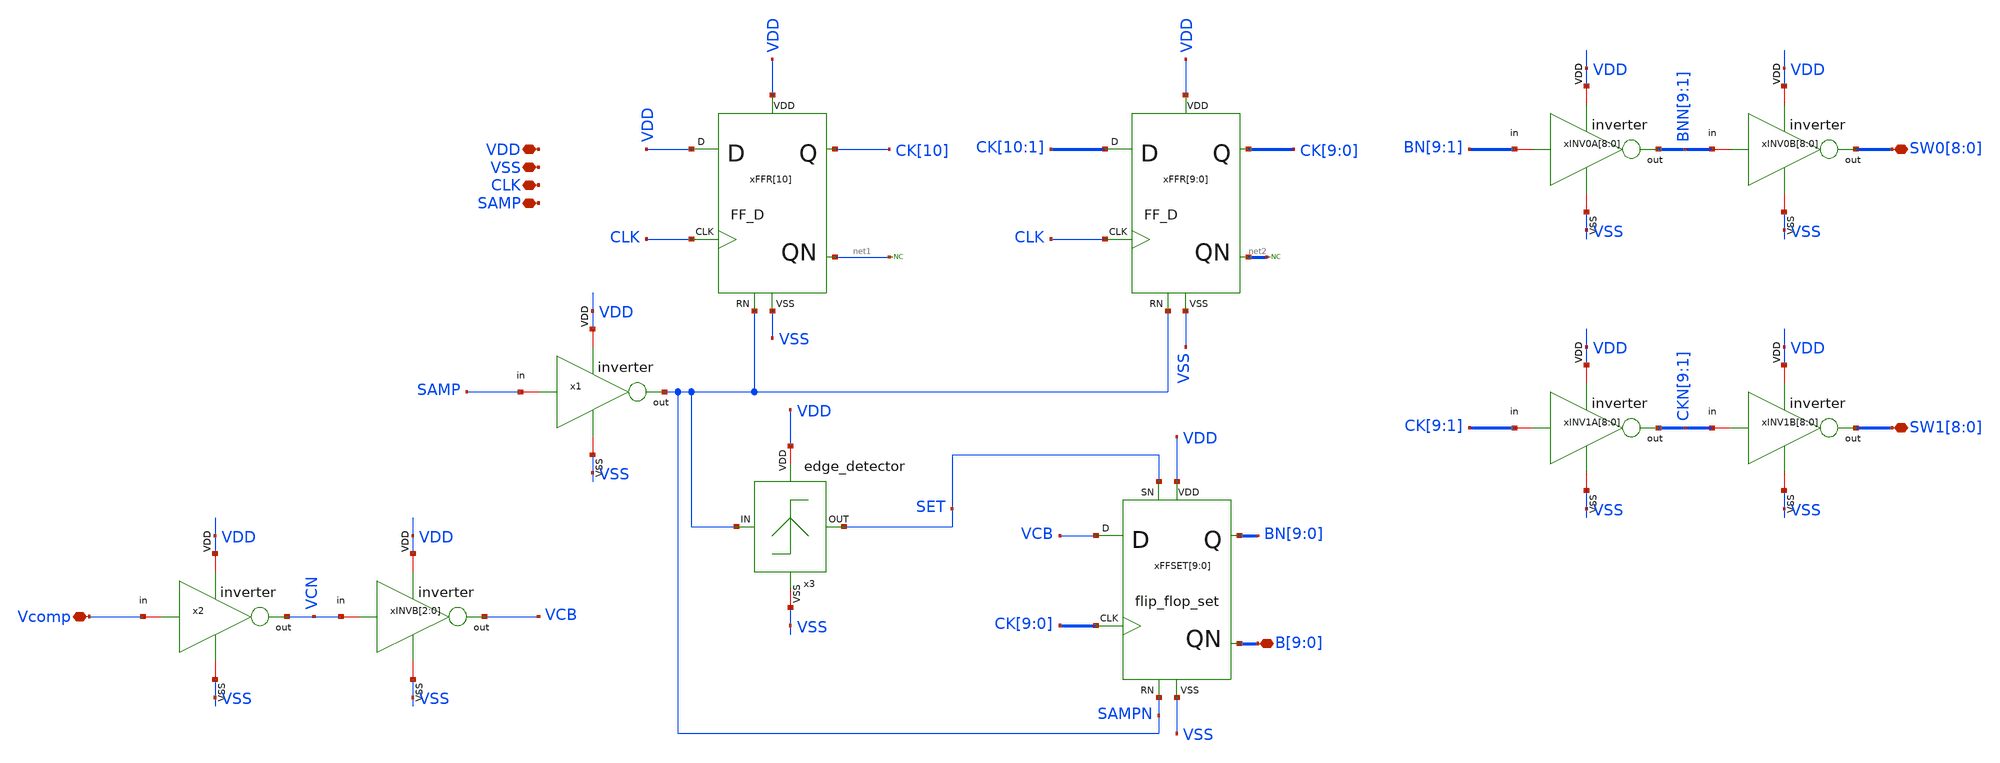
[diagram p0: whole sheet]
** sch_path: designs/sar_adc/digital/logica_digital_TOP/xschem/logica_digital_TOP.sch
**.subckt logica_digital_TOP VDD VSS SAMP CLK Vcomp
*+ B[9],B[8],B[7],B[6],B[5],B[4],B[3],B[2],B[1],B[0] SW0[8],SW0[7],SW0[6],SW0[5],SW0[4],SW0[3],SW0[2],SW0[1],SW0[0]
*+ SW1[8],SW1[7],SW1[6],SW1[5],SW1[4],SW1[3],SW1[2],SW1[1],SW1[0]
*.iopin VDD
*.iopin VSS
*.iopin SAMP
*.iopin CLK
*.iopin Vcomp
*.iopin B[9],B[8],B[7],B[6],B[5],B[4],B[3],B[2],B[1],B[0]
*.iopin SW0[8],SW0[7],SW0[6],SW0[5],SW0[4],SW0[3],SW0[2],SW0[1],SW0[0]
*.iopin SW1[8],SW1[7],SW1[6],SW1[5],SW1[4],SW1[3],SW1[2],SW1[1],SW1[0]
xFFR[10] CLK VDD VDD VSS CK[10] SAMPN net1 FF_D
xFFR[9] CLK CK[10] VDD VSS CK[9] SAMPN net2[9] FF_D
xFFR[8] CLK CK[9] VDD VSS CK[8] SAMPN net2[8] FF_D
xFFR[7] CLK CK[8] VDD VSS CK[7] SAMPN net2[7] FF_D
xFFR[6] CLK CK[7] VDD VSS CK[6] SAMPN net2[6] FF_D
xFFR[5] CLK CK[6] VDD VSS CK[5] SAMPN net2[5] FF_D
xFFR[4] CLK CK[5] VDD VSS CK[4] SAMPN net2[4] FF_D
xFFR[3] CLK CK[4] VDD VSS CK[3] SAMPN net2[3] FF_D
xFFR[2] CLK CK[3] VDD VSS CK[2] SAMPN net2[2] FF_D
xFFR[1] CLK CK[2] VDD VSS CK[1] SAMPN net2[1] FF_D
xFFR[0] CLK CK[1] VDD VSS CK[0] SAMPN net2[0] FF_D
xFFSET[9] CK[9] VCB VDD VSS BN[9] SAMPN B[9] SET flip_flop_set
xFFSET[8] CK[8] VCB VDD VSS BN[8] SAMPN B[8] SET flip_flop_set
xFFSET[7] CK[7] VCB VDD VSS BN[7] SAMPN B[7] SET flip_flop_set
xFFSET[6] CK[6] VCB VDD VSS BN[6] SAMPN B[6] SET flip_flop_set
xFFSET[5] CK[5] VCB VDD VSS BN[5] SAMPN B[5] SET flip_flop_set
xFFSET[4] CK[4] VCB VDD VSS BN[4] SAMPN B[4] SET flip_flop_set
xFFSET[3] CK[3] VCB VDD VSS BN[3] SAMPN B[3] SET flip_flop_set
xFFSET[2] CK[2] VCB VDD VSS BN[2] SAMPN B[2] SET flip_flop_set
xFFSET[1] CK[1] VCB VDD VSS BN[1] SAMPN B[1] SET flip_flop_set
xFFSET[0] CK[0] VCB VDD VSS BN[0] SAMPN B[0] SET flip_flop_set
x3 SAMPN SET VDD VSS edge_detector
* noconn #net2
x1 VDD SAMP SAMPN VSS inverter
* noconn #net1
x2 VDD Vcomp VCN VSS inverter
xINVB[2] VDD VCN VCB VSS inverter
xINVB[1] VDD VCN VCB VSS inverter
xINVB[0] VDD VCN VCB VSS inverter
xINV0A[8] VDD BN[9] BNN[9] VSS inverter
xINV0A[7] VDD BN[8] BNN[8] VSS inverter
xINV0A[6] VDD BN[7] BNN[7] VSS inverter
xINV0A[5] VDD BN[6] BNN[6] VSS inverter
xINV0A[4] VDD BN[5] BNN[5] VSS inverter
xINV0A[3] VDD BN[4] BNN[4] VSS inverter
xINV0A[2] VDD BN[3] BNN[3] VSS inverter
xINV0A[1] VDD BN[2] BNN[2] VSS inverter
xINV0A[0] VDD BN[1] BNN[1] VSS inverter
xINV0B[8] VDD BNN[9] SW0[8] VSS inverter
xINV0B[7] VDD BNN[8] SW0[7] VSS inverter
xINV0B[6] VDD BNN[7] SW0[6] VSS inverter
xINV0B[5] VDD BNN[6] SW0[5] VSS inverter
xINV0B[4] VDD BNN[5] SW0[4] VSS inverter
xINV0B[3] VDD BNN[4] SW0[3] VSS inverter
xINV0B[2] VDD BNN[3] SW0[2] VSS inverter
xINV0B[1] VDD BNN[2] SW0[1] VSS inverter
xINV0B[0] VDD BNN[1] SW0[0] VSS inverter
xINV1A[8] VDD CK[9] CKN[9] VSS inverter
xINV1A[7] VDD CK[8] CKN[8] VSS inverter
xINV1A[6] VDD CK[7] CKN[7] VSS inverter
xINV1A[5] VDD CK[6] CKN[6] VSS inverter
xINV1A[4] VDD CK[5] CKN[5] VSS inverter
xINV1A[3] VDD CK[4] CKN[4] VSS inverter
xINV1A[2] VDD CK[3] CKN[3] VSS inverter
xINV1A[1] VDD CK[2] CKN[2] VSS inverter
xINV1A[0] VDD CK[1] CKN[1] VSS inverter
xINV1B[8] VDD CKN[9] SW1[8] VSS inverter
xINV1B[7] VDD CKN[8] SW1[7] VSS inverter
xINV1B[6] VDD CKN[7] SW1[6] VSS inverter
xINV1B[5] VDD CKN[6] SW1[5] VSS inverter
xINV1B[4] VDD CKN[5] SW1[4] VSS inverter
xINV1B[3] VDD CKN[4] SW1[3] VSS inverter
xINV1B[2] VDD CKN[3] SW1[2] VSS inverter
xINV1B[1] VDD CKN[2] SW1[1] VSS inverter
xINV1B[0] VDD CKN[1] SW1[0] VSS inverter
**.ends
.end
